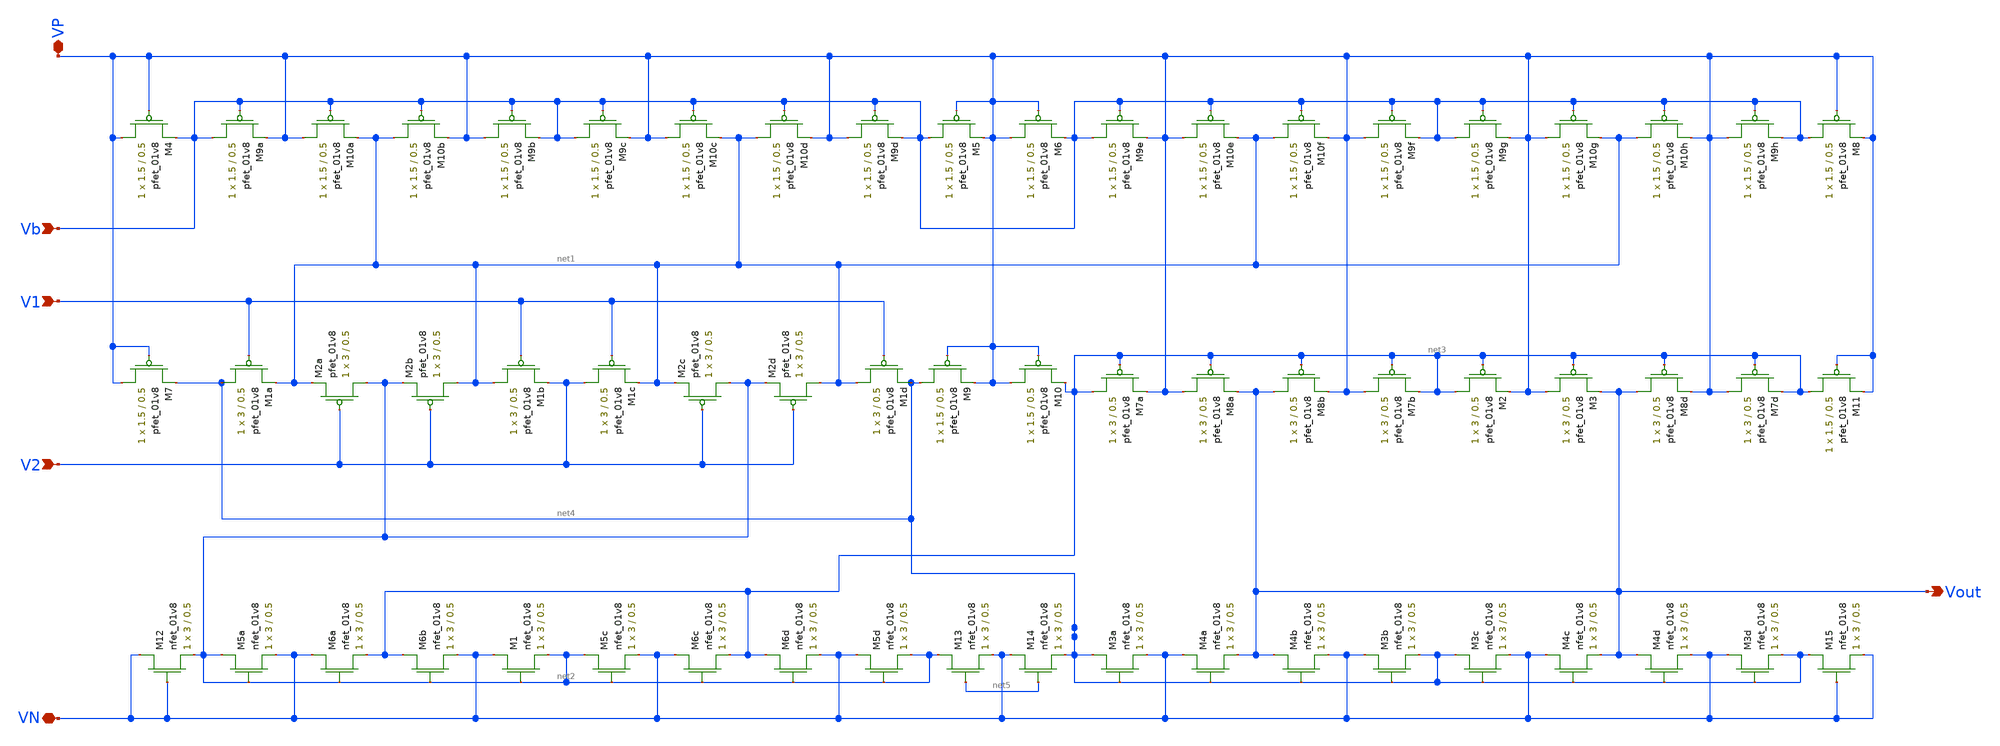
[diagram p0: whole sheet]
** sch_path: Miniproject3/cmdiffamp-test.sch
**.subckt cmdiffamp-test Vout Vb VN V1 V2 VP
*.opin Vout
*.ipin Vb
*.iopin VN
*.ipin V1
*.ipin V2
*.iopin VP
XM1a net4 V1 net1 VDD sky130_fd_pr__pfet_01v8 L=0.5 W=3 nf=1 ad='int((nf+1)/2) * W/nf * 0.29' as='int((nf+2)/2) * W/nf * 0.29'
+ pd='2*int((nf+1)/2) * (W/nf + 0.29)' ps='2*int((nf+2)/2) * (W/nf + 0.29)' nrd='0.29 / W' nrs='0.29 / W'
+ sa=0 sb=0 sd=0 mult=1 m=1
XM2a net2 V2 net1 VDD sky130_fd_pr__pfet_01v8 L=0.5 W=3 nf=1 ad='int((nf+1)/2) * W/nf * 0.29' as='int((nf+2)/2) * W/nf * 0.29'
+ pd='2*int((nf+1)/2) * (W/nf + 0.29)' ps='2*int((nf+2)/2) * (W/nf + 0.29)' nrd='0.29 / W' nrs='0.29 / W'
+ sa=0 sb=0 sd=0 mult=1 m=1
XM2b net1 V2 net2 VDD sky130_fd_pr__pfet_01v8 L=0.5 W=3 nf=1 ad='int((nf+1)/2) * W/nf * 0.29' as='int((nf+2)/2) * W/nf * 0.29'
+ pd='2*int((nf+1)/2) * (W/nf + 0.29)' ps='2*int((nf+2)/2) * (W/nf + 0.29)' nrd='0.29 / W' nrs='0.29 / W'
+ sa=0 sb=0 sd=0 mult=1 m=1
XM1b net1 V1 V2 VDD sky130_fd_pr__pfet_01v8 L=0.5 W=3 nf=1 ad='int((nf+1)/2) * W/nf * 0.29' as='int((nf+2)/2) * W/nf * 0.29'
+ pd='2*int((nf+1)/2) * (W/nf + 0.29)' ps='2*int((nf+2)/2) * (W/nf + 0.29)' nrd='0.29 / W' nrs='0.29 / W'
+ sa=0 sb=0 sd=0 mult=1 m=1
XM1c V2 V1 net1 VDD sky130_fd_pr__pfet_01v8 L=0.5 W=3 nf=1 ad='int((nf+1)/2) * W/nf * 0.29' as='int((nf+2)/2) * W/nf * 0.29'
+ pd='2*int((nf+1)/2) * (W/nf + 0.29)' ps='2*int((nf+2)/2) * (W/nf + 0.29)' nrd='0.29 / W' nrs='0.29 / W'
+ sa=0 sb=0 sd=0 mult=1 m=1
XM2c net2 V2 net1 VDD sky130_fd_pr__pfet_01v8 L=0.5 W=3 nf=1 ad='int((nf+1)/2) * W/nf * 0.29' as='int((nf+2)/2) * W/nf * 0.29'
+ pd='2*int((nf+1)/2) * (W/nf + 0.29)' ps='2*int((nf+2)/2) * (W/nf + 0.29)' nrd='0.29 / W' nrs='0.29 / W'
+ sa=0 sb=0 sd=0 mult=1 m=1
XM2d net1 V2 net2 VDD sky130_fd_pr__pfet_01v8 L=0.5 W=3 nf=1 ad='int((nf+1)/2) * W/nf * 0.29' as='int((nf+2)/2) * W/nf * 0.29'
+ pd='2*int((nf+1)/2) * (W/nf + 0.29)' ps='2*int((nf+2)/2) * (W/nf + 0.29)' nrd='0.29 / W' nrs='0.29 / W'
+ sa=0 sb=0 sd=0 mult=1 m=1
XM1d net1 V1 net4 VDD sky130_fd_pr__pfet_01v8 L=0.5 W=3 nf=1 ad='int((nf+1)/2) * W/nf * 0.29' as='int((nf+2)/2) * W/nf * 0.29'
+ pd='2*int((nf+1)/2) * (W/nf + 0.29)' ps='2*int((nf+2)/2) * (W/nf + 0.29)' nrd='0.29 / W' nrs='0.29 / W'
+ sa=0 sb=0 sd=0 mult=1 m=1
XM5a net2 net2 VN GND sky130_fd_pr__nfet_01v8 L=0.5 W=3 nf=1 ad='int((nf+1)/2) * W/nf * 0.29' as='int((nf+2)/2) * W/nf * 0.29'
+ pd='2*int((nf+1)/2) * (W/nf + 0.29)' ps='2*int((nf+2)/2) * (W/nf + 0.29)' nrd='0.29 / W' nrs='0.29 / W'
+ sa=0 sb=0 sd=0 mult=1 m=1
XM6a VN net2 net3 GND sky130_fd_pr__nfet_01v8 L=0.5 W=3 nf=1 ad='int((nf+1)/2) * W/nf * 0.29' as='int((nf+2)/2) * W/nf * 0.29'
+ pd='2*int((nf+1)/2) * (W/nf + 0.29)' ps='2*int((nf+2)/2) * (W/nf + 0.29)' nrd='0.29 / W' nrs='0.29 / W'
+ sa=0 sb=0 sd=0 mult=1 m=1
XM6b net3 net2 VN GND sky130_fd_pr__nfet_01v8 L=0.5 W=3 nf=1 ad='int((nf+1)/2) * W/nf * 0.29' as='int((nf+2)/2) * W/nf * 0.29'
+ pd='2*int((nf+1)/2) * (W/nf + 0.29)' ps='2*int((nf+2)/2) * (W/nf + 0.29)' nrd='0.29 / W' nrs='0.29 / W'
+ sa=0 sb=0 sd=0 mult=1 m=1
XM1 VN net2 net2 GND sky130_fd_pr__nfet_01v8 L=0.5 W=3 nf=1 ad='int((nf+1)/2) * W/nf * 0.29' as='int((nf+2)/2) * W/nf * 0.29'
+ pd='2*int((nf+1)/2) * (W/nf + 0.29)' ps='2*int((nf+2)/2) * (W/nf + 0.29)' nrd='0.29 / W' nrs='0.29 / W'
+ sa=0 sb=0 sd=0 mult=1 m=1
XM5c net2 net2 VN GND sky130_fd_pr__nfet_01v8 L=0.5 W=3 nf=1 ad='int((nf+1)/2) * W/nf * 0.29' as='int((nf+2)/2) * W/nf * 0.29'
+ pd='2*int((nf+1)/2) * (W/nf + 0.29)' ps='2*int((nf+2)/2) * (W/nf + 0.29)' nrd='0.29 / W' nrs='0.29 / W'
+ sa=0 sb=0 sd=0 mult=1 m=1
XM6c VN net2 net3 GND sky130_fd_pr__nfet_01v8 L=0.5 W=3 nf=1 ad='int((nf+1)/2) * W/nf * 0.29' as='int((nf+2)/2) * W/nf * 0.29'
+ pd='2*int((nf+1)/2) * (W/nf + 0.29)' ps='2*int((nf+2)/2) * (W/nf + 0.29)' nrd='0.29 / W' nrs='0.29 / W'
+ sa=0 sb=0 sd=0 mult=1 m=1
XM6d net3 net2 VN GND sky130_fd_pr__nfet_01v8 L=0.5 W=3 nf=1 ad='int((nf+1)/2) * W/nf * 0.29' as='int((nf+2)/2) * W/nf * 0.29'
+ pd='2*int((nf+1)/2) * (W/nf + 0.29)' ps='2*int((nf+2)/2) * (W/nf + 0.29)' nrd='0.29 / W' nrs='0.29 / W'
+ sa=0 sb=0 sd=0 mult=1 m=1
XM5d VN net2 net2 GND sky130_fd_pr__nfet_01v8 L=0.5 W=3 nf=1 ad='int((nf+1)/2) * W/nf * 0.29' as='int((nf+2)/2) * W/nf * 0.29'
+ pd='2*int((nf+1)/2) * (W/nf + 0.29)' ps='2*int((nf+2)/2) * (W/nf + 0.29)' nrd='0.29 / W' nrs='0.29 / W'
+ sa=0 sb=0 sd=0 mult=1 m=1
XM3a net4 net4 VN GND sky130_fd_pr__nfet_01v8 L=0.5 W=3 nf=1 ad='int((nf+1)/2) * W/nf * 0.29' as='int((nf+2)/2) * W/nf * 0.29'
+ pd='2*int((nf+1)/2) * (W/nf + 0.29)' ps='2*int((nf+2)/2) * (W/nf + 0.29)' nrd='0.29 / W' nrs='0.29 / W'
+ sa=0 sb=0 sd=0 mult=1 m=1
XM4a VN net4 Vout GND sky130_fd_pr__nfet_01v8 L=0.5 W=3 nf=1 ad='int((nf+1)/2) * W/nf * 0.29' as='int((nf+2)/2) * W/nf * 0.29'
+ pd='2*int((nf+1)/2) * (W/nf + 0.29)' ps='2*int((nf+2)/2) * (W/nf + 0.29)' nrd='0.29 / W' nrs='0.29 / W'
+ sa=0 sb=0 sd=0 mult=1 m=1
XM4b Vout net4 VN GND sky130_fd_pr__nfet_01v8 L=0.5 W=3 nf=1 ad='int((nf+1)/2) * W/nf * 0.29' as='int((nf+2)/2) * W/nf * 0.29'
+ pd='2*int((nf+1)/2) * (W/nf + 0.29)' ps='2*int((nf+2)/2) * (W/nf + 0.29)' nrd='0.29 / W' nrs='0.29 / W'
+ sa=0 sb=0 sd=0 mult=1 m=1
XM3b VN net4 net4 GND sky130_fd_pr__nfet_01v8 L=0.5 W=3 nf=1 ad='int((nf+1)/2) * W/nf * 0.29' as='int((nf+2)/2) * W/nf * 0.29'
+ pd='2*int((nf+1)/2) * (W/nf + 0.29)' ps='2*int((nf+2)/2) * (W/nf + 0.29)' nrd='0.29 / W' nrs='0.29 / W'
+ sa=0 sb=0 sd=0 mult=1 m=1
XM3c net4 net4 VN GND sky130_fd_pr__nfet_01v8 L=0.5 W=3 nf=1 ad='int((nf+1)/2) * W/nf * 0.29' as='int((nf+2)/2) * W/nf * 0.29'
+ pd='2*int((nf+1)/2) * (W/nf + 0.29)' ps='2*int((nf+2)/2) * (W/nf + 0.29)' nrd='0.29 / W' nrs='0.29 / W'
+ sa=0 sb=0 sd=0 mult=1 m=1
XM4c VN net4 Vout GND sky130_fd_pr__nfet_01v8 L=0.5 W=3 nf=1 ad='int((nf+1)/2) * W/nf * 0.29' as='int((nf+2)/2) * W/nf * 0.29'
+ pd='2*int((nf+1)/2) * (W/nf + 0.29)' ps='2*int((nf+2)/2) * (W/nf + 0.29)' nrd='0.29 / W' nrs='0.29 / W'
+ sa=0 sb=0 sd=0 mult=1 m=1
XM4d Vout net4 VN GND sky130_fd_pr__nfet_01v8 L=0.5 W=3 nf=1 ad='int((nf+1)/2) * W/nf * 0.29' as='int((nf+2)/2) * W/nf * 0.29'
+ pd='2*int((nf+1)/2) * (W/nf + 0.29)' ps='2*int((nf+2)/2) * (W/nf + 0.29)' nrd='0.29 / W' nrs='0.29 / W'
+ sa=0 sb=0 sd=0 mult=1 m=1
XM3d VN net4 net4 GND sky130_fd_pr__nfet_01v8 L=0.5 W=3 nf=1 ad='int((nf+1)/2) * W/nf * 0.29' as='int((nf+2)/2) * W/nf * 0.29'
+ pd='2*int((nf+1)/2) * (W/nf + 0.29)' ps='2*int((nf+2)/2) * (W/nf + 0.29)' nrd='0.29 / W' nrs='0.29 / W'
+ sa=0 sb=0 sd=0 mult=1 m=1
XM7a net3 net3 VP VDD sky130_fd_pr__pfet_01v8 L=0.5 W=3 nf=1 ad='int((nf+1)/2) * W/nf * 0.29' as='int((nf+2)/2) * W/nf * 0.29'
+ pd='2*int((nf+1)/2) * (W/nf + 0.29)' ps='2*int((nf+2)/2) * (W/nf + 0.29)' nrd='0.29 / W' nrs='0.29 / W'
+ sa=0 sb=0 sd=0 mult=1 m=1
XM8a VP net3 Vout VDD sky130_fd_pr__pfet_01v8 L=0.5 W=3 nf=1 ad='int((nf+1)/2) * W/nf * 0.29' as='int((nf+2)/2) * W/nf * 0.29'
+ pd='2*int((nf+1)/2) * (W/nf + 0.29)' ps='2*int((nf+2)/2) * (W/nf + 0.29)' nrd='0.29 / W' nrs='0.29 / W'
+ sa=0 sb=0 sd=0 mult=1 m=1
XM8b Vout net3 VP VDD sky130_fd_pr__pfet_01v8 L=0.5 W=3 nf=1 ad='int((nf+1)/2) * W/nf * 0.29' as='int((nf+2)/2) * W/nf * 0.29'
+ pd='2*int((nf+1)/2) * (W/nf + 0.29)' ps='2*int((nf+2)/2) * (W/nf + 0.29)' nrd='0.29 / W' nrs='0.29 / W'
+ sa=0 sb=0 sd=0 mult=1 m=1
XM7b VP net3 net3 VDD sky130_fd_pr__pfet_01v8 L=0.5 W=3 nf=1 ad='int((nf+1)/2) * W/nf * 0.29' as='int((nf+2)/2) * W/nf * 0.29'
+ pd='2*int((nf+1)/2) * (W/nf + 0.29)' ps='2*int((nf+2)/2) * (W/nf + 0.29)' nrd='0.29 / W' nrs='0.29 / W'
+ sa=0 sb=0 sd=0 mult=1 m=1
XM2 net3 net3 VP VDD sky130_fd_pr__pfet_01v8 L=0.5 W=3 nf=1 ad='int((nf+1)/2) * W/nf * 0.29' as='int((nf+2)/2) * W/nf * 0.29'
+ pd='2*int((nf+1)/2) * (W/nf + 0.29)' ps='2*int((nf+2)/2) * (W/nf + 0.29)' nrd='0.29 / W' nrs='0.29 / W'
+ sa=0 sb=0 sd=0 mult=1 m=1
XM3 VP net3 Vout VDD sky130_fd_pr__pfet_01v8 L=0.5 W=3 nf=1 ad='int((nf+1)/2) * W/nf * 0.29' as='int((nf+2)/2) * W/nf * 0.29'
+ pd='2*int((nf+1)/2) * (W/nf + 0.29)' ps='2*int((nf+2)/2) * (W/nf + 0.29)' nrd='0.29 / W' nrs='0.29 / W'
+ sa=0 sb=0 sd=0 mult=1 m=1
XM8d Vout net3 VP VDD sky130_fd_pr__pfet_01v8 L=0.5 W=3 nf=1 ad='int((nf+1)/2) * W/nf * 0.29' as='int((nf+2)/2) * W/nf * 0.29'
+ pd='2*int((nf+1)/2) * (W/nf + 0.29)' ps='2*int((nf+2)/2) * (W/nf + 0.29)' nrd='0.29 / W' nrs='0.29 / W'
+ sa=0 sb=0 sd=0 mult=1 m=1
XM7d VP net3 net3 VDD sky130_fd_pr__pfet_01v8 L=0.5 W=3 nf=1 ad='int((nf+1)/2) * W/nf * 0.29' as='int((nf+2)/2) * W/nf * 0.29'
+ pd='2*int((nf+1)/2) * (W/nf + 0.29)' ps='2*int((nf+2)/2) * (W/nf + 0.29)' nrd='0.29 / W' nrs='0.29 / W'
+ sa=0 sb=0 sd=0 mult=1 m=1
XM9a Vb Vb VP VDD sky130_fd_pr__pfet_01v8 L=0.5 W=1.5 nf=1 ad='int((nf+1)/2) * W/nf * 0.29' as='int((nf+2)/2) * W/nf * 0.29'
+ pd='2*int((nf+1)/2) * (W/nf + 0.29)' ps='2*int((nf+2)/2) * (W/nf + 0.29)' nrd='0.29 / W' nrs='0.29 / W'
+ sa=0 sb=0 sd=0 mult=1 m=1
XM10a VP Vb net1 VDD sky130_fd_pr__pfet_01v8 L=0.5 W=1.5 nf=1 ad='int((nf+1)/2) * W/nf * 0.29' as='int((nf+2)/2) * W/nf * 0.29'
+ pd='2*int((nf+1)/2) * (W/nf + 0.29)' ps='2*int((nf+2)/2) * (W/nf + 0.29)' nrd='0.29 / W' nrs='0.29 / W'
+ sa=0 sb=0 sd=0 mult=1 m=1
XM10b net1 Vb VP VDD sky130_fd_pr__pfet_01v8 L=0.5 W=1.5 nf=1 ad='int((nf+1)/2) * W/nf * 0.29' as='int((nf+2)/2) * W/nf * 0.29'
+ pd='2*int((nf+1)/2) * (W/nf + 0.29)' ps='2*int((nf+2)/2) * (W/nf + 0.29)' nrd='0.29 / W' nrs='0.29 / W'
+ sa=0 sb=0 sd=0 mult=1 m=1
XM9b VP Vb Vb VDD sky130_fd_pr__pfet_01v8 L=0.5 W=1.5 nf=1 ad='int((nf+1)/2) * W/nf * 0.29' as='int((nf+2)/2) * W/nf * 0.29'
+ pd='2*int((nf+1)/2) * (W/nf + 0.29)' ps='2*int((nf+2)/2) * (W/nf + 0.29)' nrd='0.29 / W' nrs='0.29 / W'
+ sa=0 sb=0 sd=0 mult=1 m=1
XM9c Vb Vb VP VDD sky130_fd_pr__pfet_01v8 L=0.5 W=1.5 nf=1 ad='int((nf+1)/2) * W/nf * 0.29' as='int((nf+2)/2) * W/nf * 0.29'
+ pd='2*int((nf+1)/2) * (W/nf + 0.29)' ps='2*int((nf+2)/2) * (W/nf + 0.29)' nrd='0.29 / W' nrs='0.29 / W'
+ sa=0 sb=0 sd=0 mult=1 m=1
XM10c VP Vb net1 VDD sky130_fd_pr__pfet_01v8 L=0.5 W=1.5 nf=1 ad='int((nf+1)/2) * W/nf * 0.29' as='int((nf+2)/2) * W/nf * 0.29'
+ pd='2*int((nf+1)/2) * (W/nf + 0.29)' ps='2*int((nf+2)/2) * (W/nf + 0.29)' nrd='0.29 / W' nrs='0.29 / W'
+ sa=0 sb=0 sd=0 mult=1 m=1
XM10d net1 Vb VP VDD sky130_fd_pr__pfet_01v8 L=0.5 W=1.5 nf=1 ad='int((nf+1)/2) * W/nf * 0.29' as='int((nf+2)/2) * W/nf * 0.29'
+ pd='2*int((nf+1)/2) * (W/nf + 0.29)' ps='2*int((nf+2)/2) * (W/nf + 0.29)' nrd='0.29 / W' nrs='0.29 / W'
+ sa=0 sb=0 sd=0 mult=1 m=1
XM9d VP Vb Vb VDD sky130_fd_pr__pfet_01v8 L=0.5 W=1.5 nf=1 ad='int((nf+1)/2) * W/nf * 0.29' as='int((nf+2)/2) * W/nf * 0.29'
+ pd='2*int((nf+1)/2) * (W/nf + 0.29)' ps='2*int((nf+2)/2) * (W/nf + 0.29)' nrd='0.29 / W' nrs='0.29 / W'
+ sa=0 sb=0 sd=0 mult=1 m=1
XM9e Vb Vb VP VDD sky130_fd_pr__pfet_01v8 L=0.5 W=1.5 nf=1 ad='int((nf+1)/2) * W/nf * 0.29' as='int((nf+2)/2) * W/nf * 0.29'
+ pd='2*int((nf+1)/2) * (W/nf + 0.29)' ps='2*int((nf+2)/2) * (W/nf + 0.29)' nrd='0.29 / W' nrs='0.29 / W'
+ sa=0 sb=0 sd=0 mult=1 m=1
XM10e VP Vb net1 VDD sky130_fd_pr__pfet_01v8 L=0.5 W=1.5 nf=1 ad='int((nf+1)/2) * W/nf * 0.29' as='int((nf+2)/2) * W/nf * 0.29'
+ pd='2*int((nf+1)/2) * (W/nf + 0.29)' ps='2*int((nf+2)/2) * (W/nf + 0.29)' nrd='0.29 / W' nrs='0.29 / W'
+ sa=0 sb=0 sd=0 mult=1 m=1
XM10f net1 Vb VP VDD sky130_fd_pr__pfet_01v8 L=0.5 W=1.5 nf=1 ad='int((nf+1)/2) * W/nf * 0.29' as='int((nf+2)/2) * W/nf * 0.29'
+ pd='2*int((nf+1)/2) * (W/nf + 0.29)' ps='2*int((nf+2)/2) * (W/nf + 0.29)' nrd='0.29 / W' nrs='0.29 / W'
+ sa=0 sb=0 sd=0 mult=1 m=1
XM9f VP Vb Vb VDD sky130_fd_pr__pfet_01v8 L=0.5 W=1.5 nf=1 ad='int((nf+1)/2) * W/nf * 0.29' as='int((nf+2)/2) * W/nf * 0.29'
+ pd='2*int((nf+1)/2) * (W/nf + 0.29)' ps='2*int((nf+2)/2) * (W/nf + 0.29)' nrd='0.29 / W' nrs='0.29 / W'
+ sa=0 sb=0 sd=0 mult=1 m=1
XM9g Vb Vb VP VDD sky130_fd_pr__pfet_01v8 L=0.5 W=1.5 nf=1 ad='int((nf+1)/2) * W/nf * 0.29' as='int((nf+2)/2) * W/nf * 0.29'
+ pd='2*int((nf+1)/2) * (W/nf + 0.29)' ps='2*int((nf+2)/2) * (W/nf + 0.29)' nrd='0.29 / W' nrs='0.29 / W'
+ sa=0 sb=0 sd=0 mult=1 m=1
XM10g VP Vb net1 VDD sky130_fd_pr__pfet_01v8 L=0.5 W=1.5 nf=1 ad='int((nf+1)/2) * W/nf * 0.29' as='int((nf+2)/2) * W/nf * 0.29'
+ pd='2*int((nf+1)/2) * (W/nf + 0.29)' ps='2*int((nf+2)/2) * (W/nf + 0.29)' nrd='0.29 / W' nrs='0.29 / W'
+ sa=0 sb=0 sd=0 mult=1 m=1
XM10h net1 Vb VP VDD sky130_fd_pr__pfet_01v8 L=0.5 W=1.5 nf=1 ad='int((nf+1)/2) * W/nf * 0.29' as='int((nf+2)/2) * W/nf * 0.29'
+ pd='2*int((nf+1)/2) * (W/nf + 0.29)' ps='2*int((nf+2)/2) * (W/nf + 0.29)' nrd='0.29 / W' nrs='0.29 / W'
+ sa=0 sb=0 sd=0 mult=1 m=1
XM9h VP Vb Vb VDD sky130_fd_pr__pfet_01v8 L=0.5 W=1.5 nf=1 ad='int((nf+1)/2) * W/nf * 0.29' as='int((nf+2)/2) * W/nf * 0.29'
+ pd='2*int((nf+1)/2) * (W/nf + 0.29)' ps='2*int((nf+2)/2) * (W/nf + 0.29)' nrd='0.29 / W' nrs='0.29 / W'
+ sa=0 sb=0 sd=0 mult=1 m=1
XM4 VP VP Vb VDD sky130_fd_pr__pfet_01v8 L=0.5 W=1.5 nf=1 ad='int((nf+1)/2) * W/nf * 0.29' as='int((nf+2)/2) * W/nf * 0.29'
+ pd='2*int((nf+1)/2) * (W/nf + 0.29)' ps='2*int((nf+2)/2) * (W/nf + 0.29)' nrd='0.29 / W' nrs='0.29 / W'
+ sa=0 sb=0 sd=0 mult=1 m=1
XM5 Vb VP VP VDD sky130_fd_pr__pfet_01v8 L=0.5 W=1.5 nf=1 ad='int((nf+1)/2) * W/nf * 0.29' as='int((nf+2)/2) * W/nf * 0.29'
+ pd='2*int((nf+1)/2) * (W/nf + 0.29)' ps='2*int((nf+2)/2) * (W/nf + 0.29)' nrd='0.29 / W' nrs='0.29 / W'
+ sa=0 sb=0 sd=0 mult=1 m=1
XM6 VP VP Vb VDD sky130_fd_pr__pfet_01v8 L=0.5 W=1.5 nf=1 ad='int((nf+1)/2) * W/nf * 0.29' as='int((nf+2)/2) * W/nf * 0.29'
+ pd='2*int((nf+1)/2) * (W/nf + 0.29)' ps='2*int((nf+2)/2) * (W/nf + 0.29)' nrd='0.29 / W' nrs='0.29 / W'
+ sa=0 sb=0 sd=0 mult=1 m=1
XM8 Vb VP VP VDD sky130_fd_pr__pfet_01v8 L=0.5 W=1.5 nf=1 ad='int((nf+1)/2) * W/nf * 0.29' as='int((nf+2)/2) * W/nf * 0.29'
+ pd='2*int((nf+1)/2) * (W/nf + 0.29)' ps='2*int((nf+2)/2) * (W/nf + 0.29)' nrd='0.29 / W' nrs='0.29 / W'
+ sa=0 sb=0 sd=0 mult=1 m=1
XM7 VP VP net4 VDD sky130_fd_pr__pfet_01v8 L=0.5 W=1.5 nf=1 ad='int((nf+1)/2) * W/nf * 0.29' as='int((nf+2)/2) * W/nf * 0.29'
+ pd='2*int((nf+1)/2) * (W/nf + 0.29)' ps='2*int((nf+2)/2) * (W/nf + 0.29)' nrd='0.29 / W' nrs='0.29 / W'
+ sa=0 sb=0 sd=0 mult=1 m=1
XM9 net4 VP VP VDD sky130_fd_pr__pfet_01v8 L=0.5 W=1.5 nf=1 ad='int((nf+1)/2) * W/nf * 0.29' as='int((nf+2)/2) * W/nf * 0.29'
+ pd='2*int((nf+1)/2) * (W/nf + 0.29)' ps='2*int((nf+2)/2) * (W/nf + 0.29)' nrd='0.29 / W' nrs='0.29 / W'
+ sa=0 sb=0 sd=0 mult=1 m=1
XM10 VP VP net3 VDD sky130_fd_pr__pfet_01v8 L=0.5 W=1.5 nf=1 ad='int((nf+1)/2) * W/nf * 0.29' as='int((nf+2)/2) * W/nf * 0.29'
+ pd='2*int((nf+1)/2) * (W/nf + 0.29)' ps='2*int((nf+2)/2) * (W/nf + 0.29)' nrd='0.29 / W' nrs='0.29 / W'
+ sa=0 sb=0 sd=0 mult=1 m=1
XM11 net3 VP VP VDD sky130_fd_pr__pfet_01v8 L=0.5 W=1.5 nf=1 ad='int((nf+1)/2) * W/nf * 0.29' as='int((nf+2)/2) * W/nf * 0.29'
+ pd='2*int((nf+1)/2) * (W/nf + 0.29)' ps='2*int((nf+2)/2) * (W/nf + 0.29)' nrd='0.29 / W' nrs='0.29 / W'
+ sa=0 sb=0 sd=0 mult=1 m=1
XM12 VN VN net2 GND sky130_fd_pr__nfet_01v8 L=0.5 W=3 nf=1 ad='int((nf+1)/2) * W/nf * 0.29' as='int((nf+2)/2) * W/nf * 0.29'
+ pd='2*int((nf+1)/2) * (W/nf + 0.29)' ps='2*int((nf+2)/2) * (W/nf + 0.29)' nrd='0.29 / W' nrs='0.29 / W'
+ sa=0 sb=0 sd=0 mult=1 m=1
XM13 net2 net5 VN GND sky130_fd_pr__nfet_01v8 L=0.5 W=3 nf=1 ad='int((nf+1)/2) * W/nf * 0.29' as='int((nf+2)/2) * W/nf * 0.29'
+ pd='2*int((nf+1)/2) * (W/nf + 0.29)' ps='2*int((nf+2)/2) * (W/nf + 0.29)' nrd='0.29 / W' nrs='0.29 / W'
+ sa=0 sb=0 sd=0 mult=1 m=1
XM14 VN net5 net4 GND sky130_fd_pr__nfet_01v8 L=0.5 W=3 nf=1 ad='int((nf+1)/2) * W/nf * 0.29' as='int((nf+2)/2) * W/nf * 0.29'
+ pd='2*int((nf+1)/2) * (W/nf + 0.29)' ps='2*int((nf+2)/2) * (W/nf + 0.29)' nrd='0.29 / W' nrs='0.29 / W'
+ sa=0 sb=0 sd=0 mult=1 m=1
XM15 net4 VN VN GND sky130_fd_pr__nfet_01v8 L=0.5 W=3 nf=1 ad='int((nf+1)/2) * W/nf * 0.29' as='int((nf+2)/2) * W/nf * 0.29'
+ pd='2*int((nf+1)/2) * (W/nf + 0.29)' ps='2*int((nf+2)/2) * (W/nf + 0.29)' nrd='0.29 / W' nrs='0.29 / W'
+ sa=0 sb=0 sd=0 mult=1 m=1
**.ends
.end
